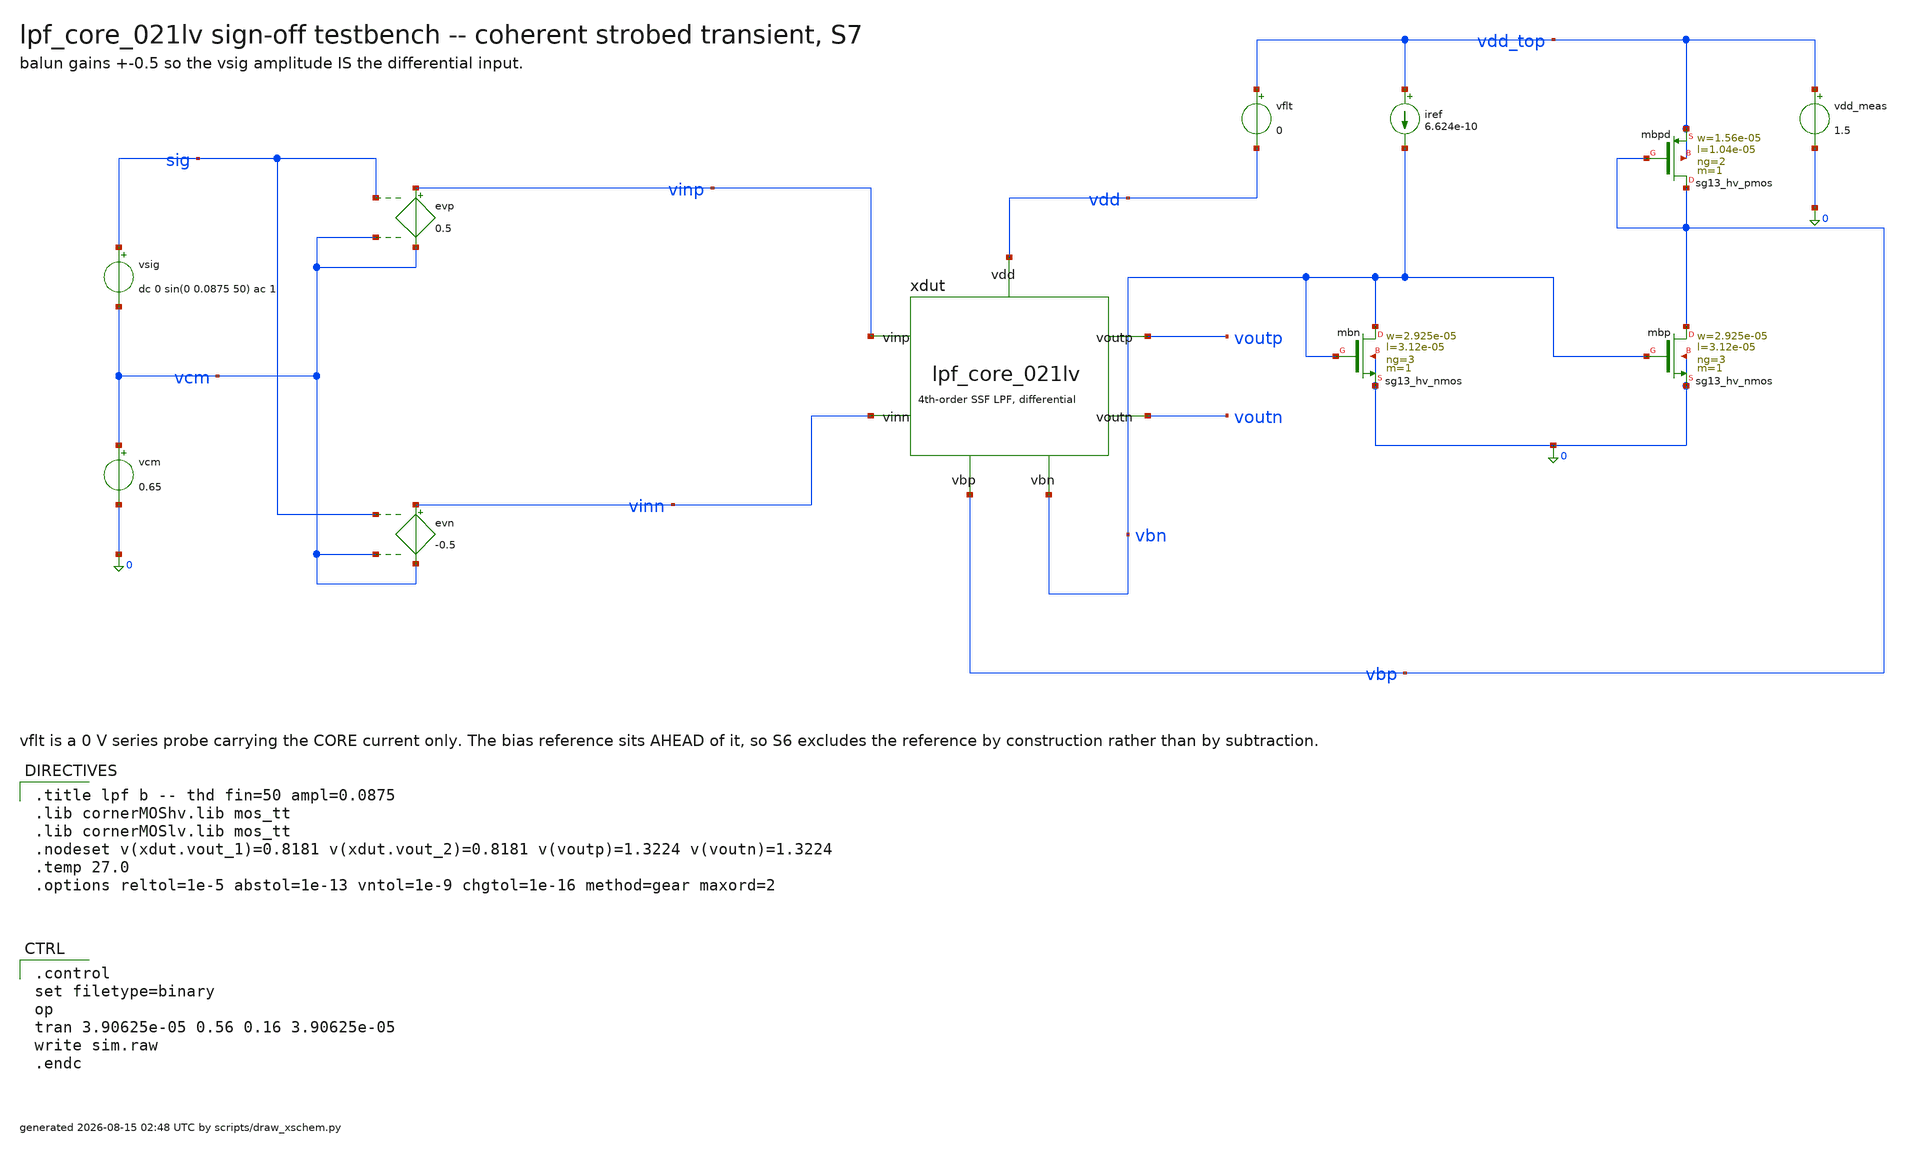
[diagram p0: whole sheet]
** sch_path: signoff/schematic/lpf_tb_021lv_thd.sch
**.subckt lpf_tb_021lv_thd
vsig sig vcm dc 0 sin(0 0.0875 50) ac 1
vcm vcm 0 0.65
evp vinp vcm sig vcm 0.5
evn vinn vcm sig vcm -0.5
xdut vinp vinn voutp voutn vbn vbp vdd lpf_core_021lv
vflt vdd_top vdd 0
vdd_meas vdd_top 0 1.5
iref vdd_top vbn 6.624e-10
Xmbn vbn vbn 0 0 sg13_hv_nmos w=2.925e-05 l=3.12e-05 ng=3 m=1 mm_ok=1
Xmbp vbp vbn 0 0 sg13_hv_nmos w=2.925e-05 l=3.12e-05 ng=3 m=1 mm_ok=1
Xmbpd vbp vbp vdd_top vdd_top sg13_hv_pmos w=1.56e-05 l=1.04e-05 ng=2 m=1 mm_ok=1
**** begin user architecture code

.title lpf b -- thd fin=50 ampl=0.0875
.lib cornerMOShv.lib mos_tt
.lib cornerMOSlv.lib mos_tt
.nodeset v(xdut.vout_1)=0.8181 v(xdut.vout_2)=0.8181 v(voutp)=1.3224 v(voutn)=1.3224
.temp 27.0
.options reltol=1e-5 abstol=1e-13 vntol=1e-9 chgtol=1e-16 method=gear maxord=2


.control
set filetype=binary
op
tran 3.90625e-05 0.56 0.16 3.90625e-05
write sim.raw
.endc

**** end user architecture code
**.ends

* expanding   symbol:  lpf_core_021lv.sym # of pins=7
** sym_path: signoff/schematic/lpf_core_021lv.sym
** sch_path: signoff/schematic/lpf_core_021lv.sch
.subckt lpf_core_021lv vinp vinn voutp voutn vbn vbp vdd
*.ipin vinp
*.ipin vinn
*.opin voutp
*.opin voutn
*.ipin vdd
*.ipin vbn
*.ipin vbp
Xm2 net2 vinp vout_1 vout_1 sg13_lv_pmos w=1.56e-05 l=1.04e-05 ng=2 m=1 mm_ok=1
Xm5 net3 vinn vout_2 vout_2 sg13_lv_pmos w=1.56e-05 l=1.04e-05 ng=2 m=1 mm_ok=1
Xm4 vout_1 net2 0 0 sg13_hv_nmos w=7.8e-06 l=5.2e-06 ng=1 m=1 mm_ok=1
Xm8 vout_2 net3 0 0 sg13_hv_nmos w=7.8e-06 l=5.2e-06 ng=1 m=1 mm_ok=1
Xm9 net2 vbn 0 0 sg13_hv_nmos w=2.925e-05 l=3.12e-05 ng=3 m=1 mm_ok=1
Xm10 net3 vbn 0 0 sg13_hv_nmos w=2.925e-05 l=3.12e-05 ng=3 m=1 mm_ok=1
Xmst vout_1 vbn net4 net4 sg13_hv_pmos w=1.62e-06 l=1.092e-05 ng=1 m=1 mm_ok=1
Xmstn vout_2 vbn net1 net1 sg13_hv_pmos w=1.62e-06 l=1.092e-05 ng=1 m=1 mm_ok=1
Xm0 net4 vout_1 voutp voutp sg13_hv_pmos w=1.56e-05 l=1.04e-05 ng=2 m=1 mm_ok=1
Xm1 net1 vout_2 voutn voutn sg13_hv_pmos w=1.56e-05 l=1.04e-05 ng=2 m=1 mm_ok=1
Xm14 voutp net4 vdd vdd sg13_hv_pmos w=8.085e-06 l=1.56e-05 ng=1 m=1 mm_ok=1
Xm15 voutn net1 vdd vdd sg13_hv_pmos w=8.085e-06 l=1.56e-05 ng=1 m=1 mm_ok=1
c13 net2 vout_1 6.58174e-12 m=1
c17 net3 vout_2 6.58174e-12 m=1
c19 vout_2 vout_1 2.65642e-11 m=1
c1 voutp net4 5.18878e-11 m=1
c10 voutn net1 5.18878e-11 m=1
c12 voutn voutp 2.04984e-11 m=1
.ends

.end
